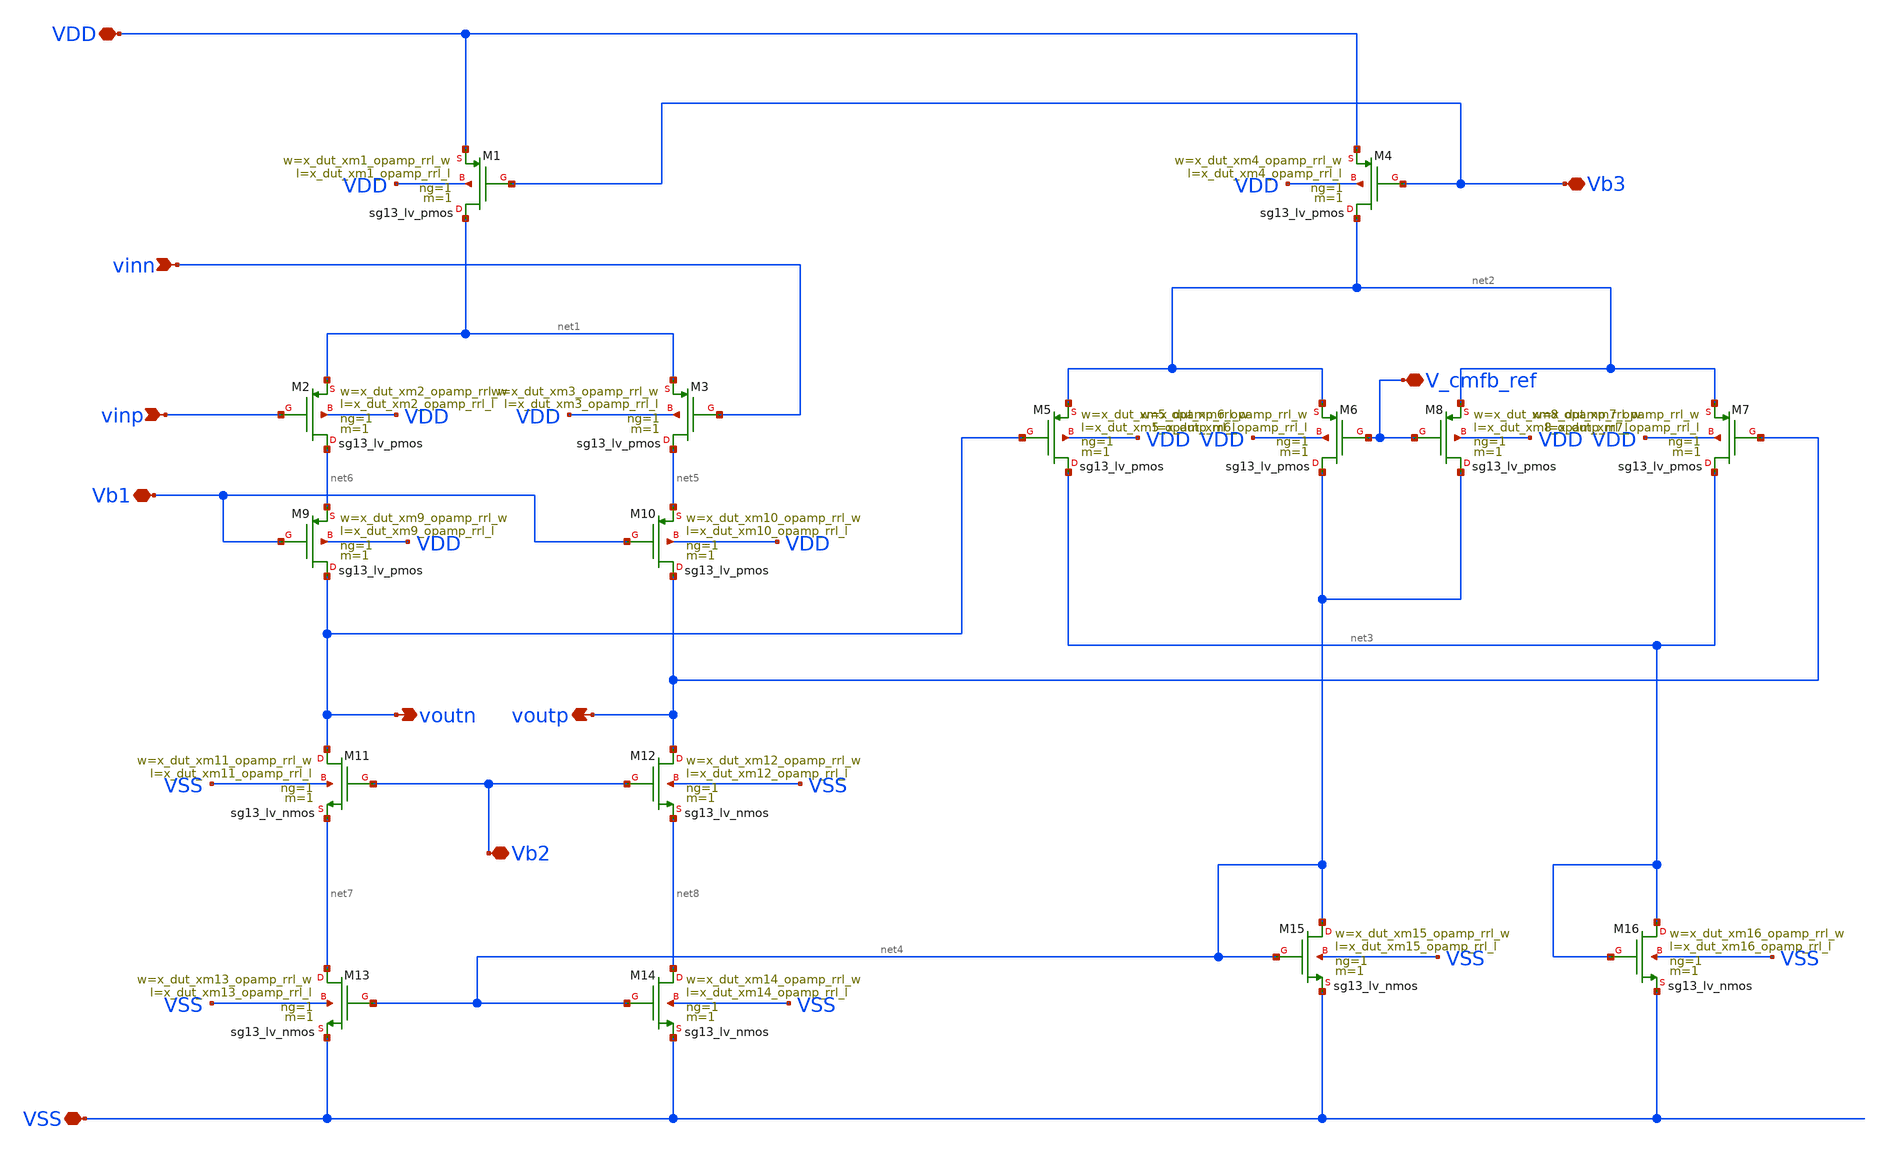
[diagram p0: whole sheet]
** sch_path: analog-db/drawings/ccia-02-QinwenFan-chopper-ripple-reduction/integrator-switchcap-opamp.sch
* Copyright 2026 MacAnalog Research Group
**.subckt integrator-switchcap-opamp VDD vinp vinn Vb3 Vb1 VSS Vb2 voutn voutp V_cmfb_ref
*.iopin VDD
*.ipin vinp
*.ipin vinn
*.iopin Vb3
*.iopin Vb1
*.iopin VSS
*.iopin Vb2
*.opin voutn
*.opin voutp
*.iopin V_cmfb_ref
XM1 net1 Vb3 VDD VDD sg13_lv_pmos w=x_dut_xm1_opamp_rrl_w l=x_dut_xm1_opamp_rrl_l ng=1 m=1 mm_ok=1
XM2 net6 vinp net1 VDD sg13_lv_pmos w=x_dut_xm2_opamp_rrl_w l=x_dut_xm2_opamp_rrl_l ng=1 m=1 mm_ok=1
XM3 net5 vinn net1 VDD sg13_lv_pmos w=x_dut_xm3_opamp_rrl_w l=x_dut_xm3_opamp_rrl_l ng=1 m=1 mm_ok=1
XM4 net2 Vb3 VDD VDD sg13_lv_pmos w=x_dut_xm4_opamp_rrl_w l=x_dut_xm4_opamp_rrl_l ng=1 m=1 mm_ok=1
XM5 net3 voutn net2 VDD sg13_lv_pmos w=x_dut_xm5_opamp_rrl_w l=x_dut_xm5_opamp_rrl_l ng=1 m=1
+ mm_ok=1
XM6 net4 V_cmfb_ref net2 VDD sg13_lv_pmos w=x_dut_xm6_opamp_rrl_w l=x_dut_xm6_opamp_rrl_l ng=1 m=1
+ mm_ok=1
XM7 net3 voutp net2 VDD sg13_lv_pmos w=x_dut_xm7_opamp_rrl_w l=x_dut_xm7_opamp_rrl_l ng=1 m=1
+ mm_ok=1
XM8 net4 V_cmfb_ref net2 VDD sg13_lv_pmos w=x_dut_xm8_opamp_rrl_w l=x_dut_xm8_opamp_rrl_l ng=1 m=1
+ mm_ok=1
XM9 voutn Vb1 net6 VDD sg13_lv_pmos w=x_dut_xm9_opamp_rrl_w l=x_dut_xm9_opamp_rrl_l ng=1 m=1 mm_ok=1
XM10 voutp Vb1 net5 VDD sg13_lv_pmos w=x_dut_xm10_opamp_rrl_w l=x_dut_xm10_opamp_rrl_l ng=1 m=1
+ mm_ok=1
XM11 voutn Vb2 net7 VSS sg13_lv_nmos w=x_dut_xm11_opamp_rrl_w l=x_dut_xm11_opamp_rrl_l ng=1 m=1
+ mm_ok=1
XM12 voutp Vb2 net8 VSS sg13_lv_nmos w=x_dut_xm12_opamp_rrl_w l=x_dut_xm12_opamp_rrl_l ng=1 m=1
+ mm_ok=1
XM13 net7 net4 VSS VSS sg13_lv_nmos w=x_dut_xm13_opamp_rrl_w l=x_dut_xm13_opamp_rrl_l ng=1 m=1
+ mm_ok=1
XM14 net8 net4 VSS VSS sg13_lv_nmos w=x_dut_xm14_opamp_rrl_w l=x_dut_xm14_opamp_rrl_l ng=1 m=1
+ mm_ok=1
XM15 net4 net4 VSS VSS sg13_lv_nmos w=x_dut_xm15_opamp_rrl_w l=x_dut_xm15_opamp_rrl_l ng=1 m=1
+ mm_ok=1
XM16 net3 net3 VSS VSS sg13_lv_nmos w=x_dut_xm16_opamp_rrl_w l=x_dut_xm16_opamp_rrl_l ng=1 m=1
+ mm_ok=1
**.ends
.end
